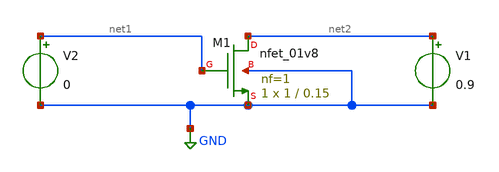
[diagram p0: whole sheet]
** sch_path: labs/xschem/netlistRcg/firstLab.sch
**.subckt firstLab
XM1 net2 net1 GND GND sky130_fd_pr__nfet_01v8 L=0.15 W=1 nf=1 ad='int((nf+1)/2) * W/nf * 0.29' as='int((nf+2)/2) * W/nf * 0.29'
+ pd='2*int((nf+1)/2) * (W/nf + 0.29)' ps='2*int((nf+2)/2) * (W/nf + 0.29)' nrd='0.29 / W' nrs='0.29 / W'
+ sa=0 sb=0 sd=0 mult=1 m=1
V1 net2 GND 0.9
V2 net1 GND 0
**** begin user architecture code



.lib /home/rcg/tools/OpenLane/OpenLane/pdks/volare/sky130/versions/e8294524e5f67c533c5d0c3afa0bcc5b2a5fa066/sky130A/libs.tech/ngspice/sky130.lib.spice tt

.control
	dc V2 0 3 0.01
	plot -i(V1)
	plot V1
.endc

.save all



**** end user architecture code
**.ends
.GLOBAL GND
.end
